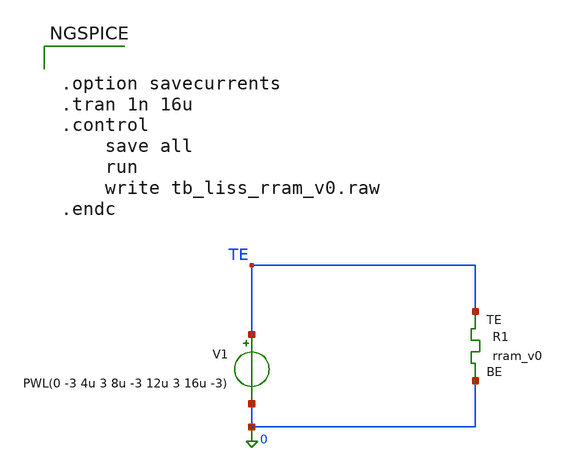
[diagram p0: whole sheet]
** sch_path: memristor_models/wellposed/tb_liss_rram_v0.sch
**.subckt tb_liss_rram_v0
V1 TE 0 PWL(0 -3 4u 3 8u -3 12u 3 16u -3)
XR1 TE 0 rram_v0
**** begin user architecture code

** opencircuitdesign pdks install
.inc $::SKYWATER_MODELS/rram_v0.spice



.option savecurrents
.tran 1n 16u
.control
	save all
	run
	write tb_liss_rram_v0.raw
.endc



**** end user architecture code
**.ends
.end
